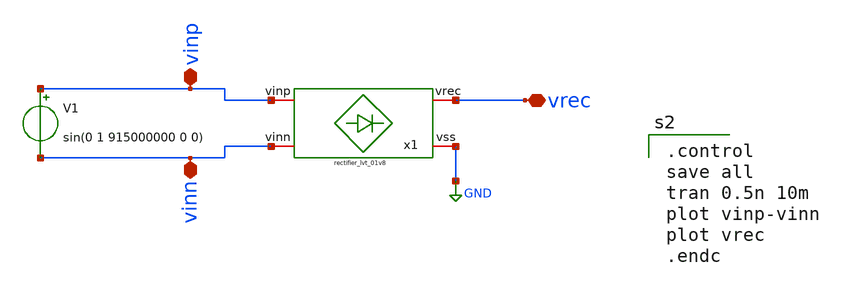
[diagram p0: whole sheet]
** sch_path: XSCHEM/rectifier_lvt_01v8_tb.sch
**.subckt rectifier_lvt_01v8_tb vrec vinp vinn
*.iopin vrec
*.iopin vinp
*.iopin vinn
V1 vinp vinn sin(0 1 915000000 0 0)
x1 vinp vrec vinn GND rectifier_lvt_01v8
**** begin user architecture code

.control
save all
tran 0.5n 10m
plot vinp-vinn
plot vrec
.endc


** opencircuitdesign pdks install
.lib $::SKYWATER_MODELS/sky130.lib.spice tt


**** end user architecture code
**.ends

* expanding   symbol:  Documentos/TESIS DE GRADO/WORK_IN_PROGRESS/My_xschem/rectifier_lvt_01v8.sym #
*+ of pins=4
** sym_path: XSCHEM/rectifier_lvt_01v8.sym
** sch_path: XSCHEM/rectifier_lvt_01v8.sch
.subckt rectifier_lvt_01v8 vinp vrec vinn vss
*.iopin vinp
*.iopin vinn
*.iopin vss
*.iopin vrec
XC11 vinp net3 sky130_fd_pr__cap_mim_m3_1 W=30 L=30 MF=1 m=1
XC12 net2 vinn sky130_fd_pr__cap_mim_m3_1 W=30 L=30 MF=1 m=1
XC13 vinp net6 sky130_fd_pr__cap_mim_m3_1 W=30 L=30 MF=1 m=1
XC14 net5 vinn sky130_fd_pr__cap_mim_m3_1 W=30 L=30 MF=1 m=1
XM25 vinp vinn vss vss sky130_fd_pr__nfet_01v8_lvt L=0.18 W=5 nf=1 ad='int((nf+1)/2) * W/nf * 0.29' as='int((nf+2)/2) * W/nf * 0.29'
+ pd='2*int((nf+1)/2) * (W/nf + 0.29)' ps='2*int((nf+2)/2) * (W/nf + 0.29)' nrd='0.29 / W' nrs='0.29 / W'
+ sa=0 sb=0 sd=0 mult=6 m=6
XM26 vinn vinp vss vss sky130_fd_pr__nfet_01v8_lvt L=0.18 W=5 nf=1 ad='int((nf+1)/2) * W/nf * 0.29' as='int((nf+2)/2) * W/nf * 0.29'
+ pd='2*int((nf+1)/2) * (W/nf + 0.29)' ps='2*int((nf+2)/2) * (W/nf + 0.29)' nrd='0.29 / W' nrs='0.29 / W'
+ sa=0 sb=0 sd=0 mult=6 m=6
XM27 vinp vinn net1 net1 sky130_fd_pr__pfet_01v8_lvt L=0.35 W=10 nf=2 ad='int((nf+1)/2) * W/nf * 0.29'
+ as='int((nf+2)/2) * W/nf * 0.29' pd='2*int((nf+1)/2) * (W/nf + 0.29)' ps='2*int((nf+2)/2) * (W/nf + 0.29)'
+ nrd='0.29 / W' nrs='0.29 / W' sa=0 sb=0 sd=0 mult=3 m=3
XM28 vinn vinp net1 net1 sky130_fd_pr__pfet_01v8_lvt L=0.35 W=10 nf=2 ad='int((nf+1)/2) * W/nf * 0.29'
+ as='int((nf+2)/2) * W/nf * 0.29' pd='2*int((nf+1)/2) * (W/nf + 0.29)' ps='2*int((nf+2)/2) * (W/nf + 0.29)'
+ nrd='0.29 / W' nrs='0.29 / W' sa=0 sb=0 sd=0 mult=3 m=3
XM29 net3 net2 net1 vss sky130_fd_pr__nfet_01v8_lvt L=0.18 W=5 nf=1 ad='int((nf+1)/2) * W/nf * 0.29'
+ as='int((nf+2)/2) * W/nf * 0.29' pd='2*int((nf+1)/2) * (W/nf + 0.29)' ps='2*int((nf+2)/2) * (W/nf + 0.29)'
+ nrd='0.29 / W' nrs='0.29 / W' sa=0 sb=0 sd=0 mult=6 m=6
XM30 net2 net3 net1 vss sky130_fd_pr__nfet_01v8_lvt L=0.18 W=5 nf=1 ad='int((nf+1)/2) * W/nf * 0.29'
+ as='int((nf+2)/2) * W/nf * 0.29' pd='2*int((nf+1)/2) * (W/nf + 0.29)' ps='2*int((nf+2)/2) * (W/nf + 0.29)'
+ nrd='0.29 / W' nrs='0.29 / W' sa=0 sb=0 sd=0 mult=6 m=6
XM31 net3 net2 net4 net4 sky130_fd_pr__pfet_01v8_lvt L=0.35 W=10 nf=2 ad='int((nf+1)/2) * W/nf * 0.29'
+ as='int((nf+2)/2) * W/nf * 0.29' pd='2*int((nf+1)/2) * (W/nf + 0.29)' ps='2*int((nf+2)/2) * (W/nf + 0.29)'
+ nrd='0.29 / W' nrs='0.29 / W' sa=0 sb=0 sd=0 mult=3 m=3
XM32 net2 net3 net4 net4 sky130_fd_pr__pfet_01v8_lvt L=0.35 W=10 nf=2 ad='int((nf+1)/2) * W/nf * 0.29'
+ as='int((nf+2)/2) * W/nf * 0.29' pd='2*int((nf+1)/2) * (W/nf + 0.29)' ps='2*int((nf+2)/2) * (W/nf + 0.29)'
+ nrd='0.29 / W' nrs='0.29 / W' sa=0 sb=0 sd=0 mult=3 m=3
XM33 net6 net5 net4 vss sky130_fd_pr__nfet_01v8_lvt L=0.18 W=5 nf=1 ad='int((nf+1)/2) * W/nf * 0.29'
+ as='int((nf+2)/2) * W/nf * 0.29' pd='2*int((nf+1)/2) * (W/nf + 0.29)' ps='2*int((nf+2)/2) * (W/nf + 0.29)'
+ nrd='0.29 / W' nrs='0.29 / W' sa=0 sb=0 sd=0 mult=6 m=6
XM34 net5 net6 net4 vss sky130_fd_pr__nfet_01v8_lvt L=0.18 W=5 nf=1 ad='int((nf+1)/2) * W/nf * 0.29'
+ as='int((nf+2)/2) * W/nf * 0.29' pd='2*int((nf+1)/2) * (W/nf + 0.29)' ps='2*int((nf+2)/2) * (W/nf + 0.29)'
+ nrd='0.29 / W' nrs='0.29 / W' sa=0 sb=0 sd=0 mult=6 m=6
XM35 net6 net5 net7 net7 sky130_fd_pr__pfet_01v8_lvt L=0.35 W=10 nf=2 ad='int((nf+1)/2) * W/nf * 0.29'
+ as='int((nf+2)/2) * W/nf * 0.29' pd='2*int((nf+1)/2) * (W/nf + 0.29)' ps='2*int((nf+2)/2) * (W/nf + 0.29)'
+ nrd='0.29 / W' nrs='0.29 / W' sa=0 sb=0 sd=0 mult=3 m=3
XM36 net5 net6 net7 net7 sky130_fd_pr__pfet_01v8_lvt L=0.35 W=10 nf=2 ad='int((nf+1)/2) * W/nf * 0.29'
+ as='int((nf+2)/2) * W/nf * 0.29' pd='2*int((nf+1)/2) * (W/nf + 0.29)' ps='2*int((nf+2)/2) * (W/nf + 0.29)'
+ nrd='0.29 / W' nrs='0.29 / W' sa=0 sb=0 sd=0 mult=3 m=3
XC15 vinp net9 sky130_fd_pr__cap_mim_m3_1 W=30 L=30 MF=1 m=1
XC16 net8 vinn sky130_fd_pr__cap_mim_m3_1 W=30 L=30 MF=1 m=1
XM37 net9 net8 net7 vss sky130_fd_pr__nfet_01v8_lvt L=0.18 W=5 nf=1 ad='int((nf+1)/2) * W/nf * 0.29'
+ as='int((nf+2)/2) * W/nf * 0.29' pd='2*int((nf+1)/2) * (W/nf + 0.29)' ps='2*int((nf+2)/2) * (W/nf + 0.29)'
+ nrd='0.29 / W' nrs='0.29 / W' sa=0 sb=0 sd=0 mult=6 m=6
XM38 net8 net9 net7 vss sky130_fd_pr__nfet_01v8_lvt L=0.18 W=5 nf=1 ad='int((nf+1)/2) * W/nf * 0.29'
+ as='int((nf+2)/2) * W/nf * 0.29' pd='2*int((nf+1)/2) * (W/nf + 0.29)' ps='2*int((nf+2)/2) * (W/nf + 0.29)'
+ nrd='0.29 / W' nrs='0.29 / W' sa=0 sb=0 sd=0 mult=6 m=6
XM39 net9 net8 net10 net10 sky130_fd_pr__pfet_01v8_lvt L=0.35 W=10 nf=2 ad='int((nf+1)/2) * W/nf * 0.29'
+ as='int((nf+2)/2) * W/nf * 0.29' pd='2*int((nf+1)/2) * (W/nf + 0.29)' ps='2*int((nf+2)/2) * (W/nf + 0.29)'
+ nrd='0.29 / W' nrs='0.29 / W' sa=0 sb=0 sd=0 mult=3 m=3
XM40 net8 net9 net10 net10 sky130_fd_pr__pfet_01v8_lvt L=0.35 W=10 nf=2 ad='int((nf+1)/2) * W/nf * 0.29'
+ as='int((nf+2)/2) * W/nf * 0.29' pd='2*int((nf+1)/2) * (W/nf + 0.29)' ps='2*int((nf+2)/2) * (W/nf + 0.29)'
+ nrd='0.29 / W' nrs='0.29 / W' sa=0 sb=0 sd=0 mult=3 m=3
XC17 vinp net12 sky130_fd_pr__cap_mim_m3_1 W=30 L=30 MF=1 m=1
XC18 net11 vinn sky130_fd_pr__cap_mim_m3_1 W=30 L=30 MF=1 m=1
XM41 net12 net11 net10 vss sky130_fd_pr__nfet_01v8_lvt L=0.18 W=5 nf=1 ad='int((nf+1)/2) * W/nf * 0.29'
+ as='int((nf+2)/2) * W/nf * 0.29' pd='2*int((nf+1)/2) * (W/nf + 0.29)' ps='2*int((nf+2)/2) * (W/nf + 0.29)'
+ nrd='0.29 / W' nrs='0.29 / W' sa=0 sb=0 sd=0 mult=6 m=6
XM42 net11 net12 net10 vss sky130_fd_pr__nfet_01v8_lvt L=0.18 W=5 nf=1 ad='int((nf+1)/2) * W/nf * 0.29'
+ as='int((nf+2)/2) * W/nf * 0.29' pd='2*int((nf+1)/2) * (W/nf + 0.29)' ps='2*int((nf+2)/2) * (W/nf + 0.29)'
+ nrd='0.29 / W' nrs='0.29 / W' sa=0 sb=0 sd=0 mult=6 m=6
XM43 net12 net11 net13 net13 sky130_fd_pr__pfet_01v8_lvt L=0.35 W=10 nf=2 ad='int((nf+1)/2) * W/nf * 0.29'
+ as='int((nf+2)/2) * W/nf * 0.29' pd='2*int((nf+1)/2) * (W/nf + 0.29)' ps='2*int((nf+2)/2) * (W/nf + 0.29)'
+ nrd='0.29 / W' nrs='0.29 / W' sa=0 sb=0 sd=0 mult=3 m=3
XM44 net11 net12 net13 net13 sky130_fd_pr__pfet_01v8_lvt L=0.35 W=10 nf=2 ad='int((nf+1)/2) * W/nf * 0.29'
+ as='int((nf+2)/2) * W/nf * 0.29' pd='2*int((nf+1)/2) * (W/nf + 0.29)' ps='2*int((nf+2)/2) * (W/nf + 0.29)'
+ nrd='0.29 / W' nrs='0.29 / W' sa=0 sb=0 sd=0 mult=3 m=3
XC19 vrec vss sky130_fd_pr__cap_mim_m3_1 W=30 L=30 MF=2 m=2
XC20 vinp net15 sky130_fd_pr__cap_mim_m3_1 W=30 L=30 MF=1 m=1
XC21 net14 vinn sky130_fd_pr__cap_mim_m3_1 W=30 L=30 MF=1 m=1
XM45 net15 net14 net13 vss sky130_fd_pr__nfet_01v8_lvt L=0.18 W=5 nf=1 ad='int((nf+1)/2) * W/nf * 0.29'
+ as='int((nf+2)/2) * W/nf * 0.29' pd='2*int((nf+1)/2) * (W/nf + 0.29)' ps='2*int((nf+2)/2) * (W/nf + 0.29)'
+ nrd='0.29 / W' nrs='0.29 / W' sa=0 sb=0 sd=0 mult=6 m=6
XM46 net14 net15 net13 vss sky130_fd_pr__nfet_01v8_lvt L=0.18 W=5 nf=1 ad='int((nf+1)/2) * W/nf * 0.29'
+ as='int((nf+2)/2) * W/nf * 0.29' pd='2*int((nf+1)/2) * (W/nf + 0.29)' ps='2*int((nf+2)/2) * (W/nf + 0.29)'
+ nrd='0.29 / W' nrs='0.29 / W' sa=0 sb=0 sd=0 mult=6 m=6
XM47 net15 net14 vrec vrec sky130_fd_pr__pfet_01v8_lvt L=0.35 W=10 nf=2 ad='int((nf+1)/2) * W/nf * 0.29'
+ as='int((nf+2)/2) * W/nf * 0.29' pd='2*int((nf+1)/2) * (W/nf + 0.29)' ps='2*int((nf+2)/2) * (W/nf + 0.29)'
+ nrd='0.29 / W' nrs='0.29 / W' sa=0 sb=0 sd=0 mult=3 m=3
XM48 net14 net15 vrec vrec sky130_fd_pr__pfet_01v8_lvt L=0.35 W=10 nf=2 ad='int((nf+1)/2) * W/nf * 0.29'
+ as='int((nf+2)/2) * W/nf * 0.29' pd='2*int((nf+1)/2) * (W/nf + 0.29)' ps='2*int((nf+2)/2) * (W/nf + 0.29)'
+ nrd='0.29 / W' nrs='0.29 / W' sa=0 sb=0 sd=0 mult=3 m=3
.ends

.GLOBAL GND
.end
